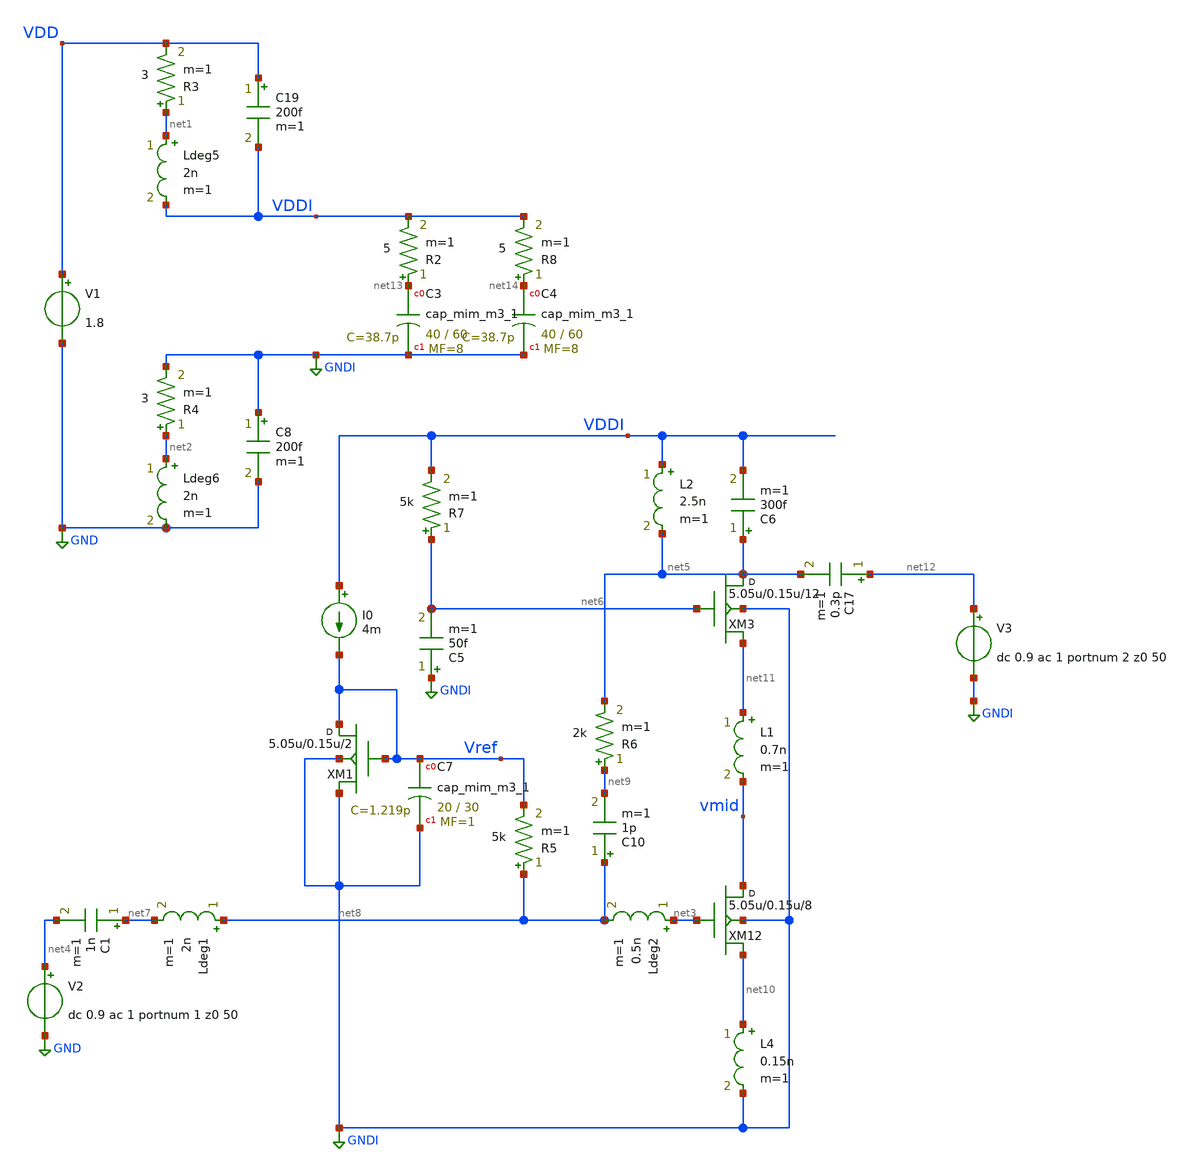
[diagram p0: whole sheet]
** sch_path: xschem/LNA5_with_output_buf_4_SP_PEX_TOP.sch
**.subckt LNA5_with_output_buf_4_SP_PEX_TOP
V1 VDD GND 1.8
V2 net4 GND dc 0.9 ac 1 portnum 1 z0 50
I0 VDDI Vref 4m
XM1 Vref Vref GNDI GNDI sky130_fd_pr__rf_nfet_01v8_bM04W5p00L0p15_ext w=5.05u l=0.15u m=2
XC7 Vref GNDI sky130_fd_pr__cap_mim_m3_1 W=20 L=30 MF=1 m=1
Ldeg5 net1 VDDI 2n m=1
R3 net1 VDD 3 m=1
Ldeg6 net2 GND 2n m=1
R4 net2 GNDI 3 m=1
XM12 vmid net3 net10 GNDI sky130_fd_pr__rf_nfet_01v8_bM04W5p00L0p15_ext w=5.05u l=0.15u m=8
C17 net12 net5 0.3p m=1
L2 VDDI net5 2.5n m=1
XC3 net13 GNDI sky130_fd_pr__cap_mim_m3_1 W=40 L=60 MF=8 m=8
C8 GNDI GND 200f m=1
C19 VDD VDDI 200f m=1
R2 net13 VDDI 5 m=1
R5 net8 Vref 5k m=1
C1 net7 net4 1n m=1
C6 net5 VDDI 300f m=1
R6 net9 net5 2k m=1
XM3 net5 net6 net11 GNDI sky130_fd_pr__rf_nfet_01v8_bM04W5p00L0p15_ext w=5.05u l=0.15u m=12
Ldeg1 net8 net7 2n m=1
L1 net11 vmid 0.7n m=1
Ldeg2 net3 net8 0.5n m=1
XC4 net14 GNDI sky130_fd_pr__cap_mim_m3_1 W=40 L=60 MF=8 m=8
R8 net14 VDDI 5 m=1
C10 net8 net9 1p m=1
L4 net10 GNDI 0.15n m=1
V3 net12 GNDI dc 0.9 ac 1 portnum 2 z0 50
R7 net6 VDDI 5k m=1
C5 GNDI net6 50f m=1
**** begin user architecture code


.subckt sky130_fd_pr__rf_nfet_01v8_bM04W5p00L0p15_ext DRAIN GATE SOURCE SUBSTRATE
X0 DRAIN GATE SOURCE SUBSTRATE sky130_fd_pr__nfet_01v8 ad=2.828e+12p pd=2.132e+07u as=4.242e+12p
+ ps=3.198e+07u w=5.05e+06u l=150000u
X1 SOURCE SUBSTRATE SUBSTRATE SUBSTRATE sky130_fd_pr__nfet_01v8 ad=0p pd=0u as=3.03e+12p
+ ps=2.14e+07u w=5.05e+06u l=150000u
X2 SOURCE GATE DRAIN SUBSTRATE sky130_fd_pr__nfet_01v8 ad=0p pd=0u as=0p ps=0u w=5.05e+06u l=150000u
X3 DRAIN GATE SOURCE SUBSTRATE sky130_fd_pr__nfet_01v8 ad=0p pd=0u as=0p ps=0u w=5.05e+06u l=150000u
X4 SUBSTRATE SUBSTRATE SOURCE SUBSTRATE sky130_fd_pr__nfet_01v8 ad=0p pd=0u as=0p ps=0u w=5.05e+06u
+ l=150000u
X5 SOURCE GATE DRAIN SUBSTRATE sky130_fd_pr__nfet_01v8 ad=0p pd=0u as=0p ps=0u w=5.05e+06u l=150000u
.ends
.sp dec 1000 0.1e9 100e9 1
* .ac dec 1000 0.01e9 100e9
.control
run
display
let z11=50*(1+s_1_1)/(1-s_1_1)
let z22=50*(1+s_2_2)/(1-s_2_2)
let S11 = S_1_1
let S21 = S_2_1
let S12 = S_1_2
let S22 = S_2_2

* Stability
let delta=S11*S22-S12*S21
let K    = (1-mag(S11)^2-mag(S22)^2+mag(delta)^2)/(2*mag(S12*S21))
let mu   = (1-mag(S11)^2)/(mag(S22-conj(S11)*delta)+mag(S21*S12))
* plot real(z11) real(z22)
* plot imag(z11) imag(z22)
plot db(S_1_1) db(S_2_2) db(S_2_1)

plot db(K)
plot mag(delta)
plot db(mu)
plot NF NFmin
.endc


.lib $::SKYWATER_MODELS/sky130.lib.spice tt
* .include $::PDKPATH/libs.ref/sky130_fd_sc_hvl/spice/sky130_fd_sc_hvl.spice

**** end user architecture code
**.ends
.GLOBAL GND
.GLOBAL GNDI
.end
